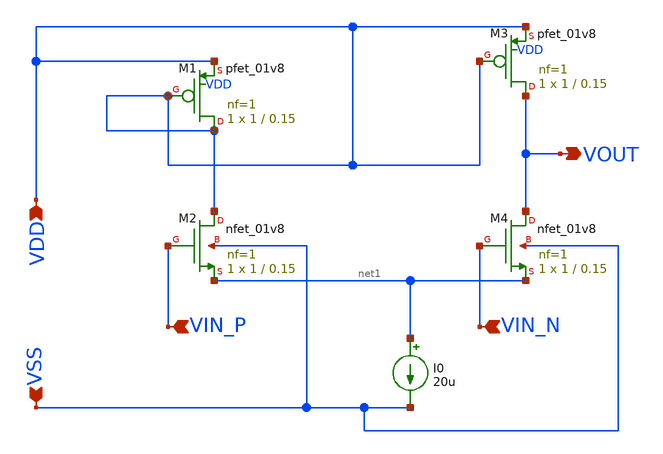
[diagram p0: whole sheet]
** sch_path: analog/build/schematic/opamp_single_stage.sch
**.subckt opamp_single_stage VIN_P VIN_N VDD VSS VOUT
*.ipin VIN_P
*.ipin VIN_N
*.ipin VDD
*.ipin VSS
*.opin VOUT
XM1 VDD VDD VDD VDD sky130_fd_pr__pfet_01v8 L=0.15 W=1 nf=1 ad='int((1 + 1)/2) * 1 / 1 * 0.29' as='int((1 + 2)/2) * 1 / 1 * 0.29'
+ pd='2*int((1 + 1)/2) * (1 / 1 + 0.29)' ps='2*int((1 + 2)/2) * (1 / 1 + 0.29)' nrd='0.29 / 1 ' nrs='0.29 / 1 '
+ sa=0 sb=0 sd=0 mult=1 m=1
XM2 VDD VIN_P net1 VSS sky130_fd_pr__nfet_01v8 L=0.15 W=1 nf=1 ad='int((1 + 1)/2) * 1 / 1 * 0.29' as='int((1 + 2)/2) * 1 / 1 * 0.29'
+ pd='2*int((1 + 1)/2) * (1 / 1 + 0.29)' ps='2*int((1 + 2)/2) * (1 / 1 + 0.29)' nrd='0.29 / 1 ' nrs='0.29 / 1 '
+ sa=0 sb=0 sd=0 mult=1 m=1
XM3 VOUT VDD VDD VDD sky130_fd_pr__pfet_01v8 L=0.15 W=1 nf=1 ad='int((1 + 1)/2) * 1 / 1 * 0.29' as='int((1 + 2)/2) * 1 / 1 * 0.29'
+ pd='2*int((1 + 1)/2) * (1 / 1 + 0.29)' ps='2*int((1 + 2)/2) * (1 / 1 + 0.29)' nrd='0.29 / 1 ' nrs='0.29 / 1 '
+ sa=0 sb=0 sd=0 mult=1 m=1
XM4 VOUT VIN_N net1 VSS sky130_fd_pr__nfet_01v8 L=0.15 W=1 nf=1 ad='int((1 + 1)/2) * 1 / 1 * 0.29' as='int((1 + 2)/2) * 1 / 1 * 0.29'
+ pd='2*int((1 + 1)/2) * (1 / 1 + 0.29)' ps='2*int((1 + 2)/2) * (1 / 1 + 0.29)' nrd='0.29 / 1 ' nrs='0.29 / 1 '
+ sa=0 sb=0 sd=0 mult=1 m=1
I0 net1 VSS 20u
**.ends
.end
